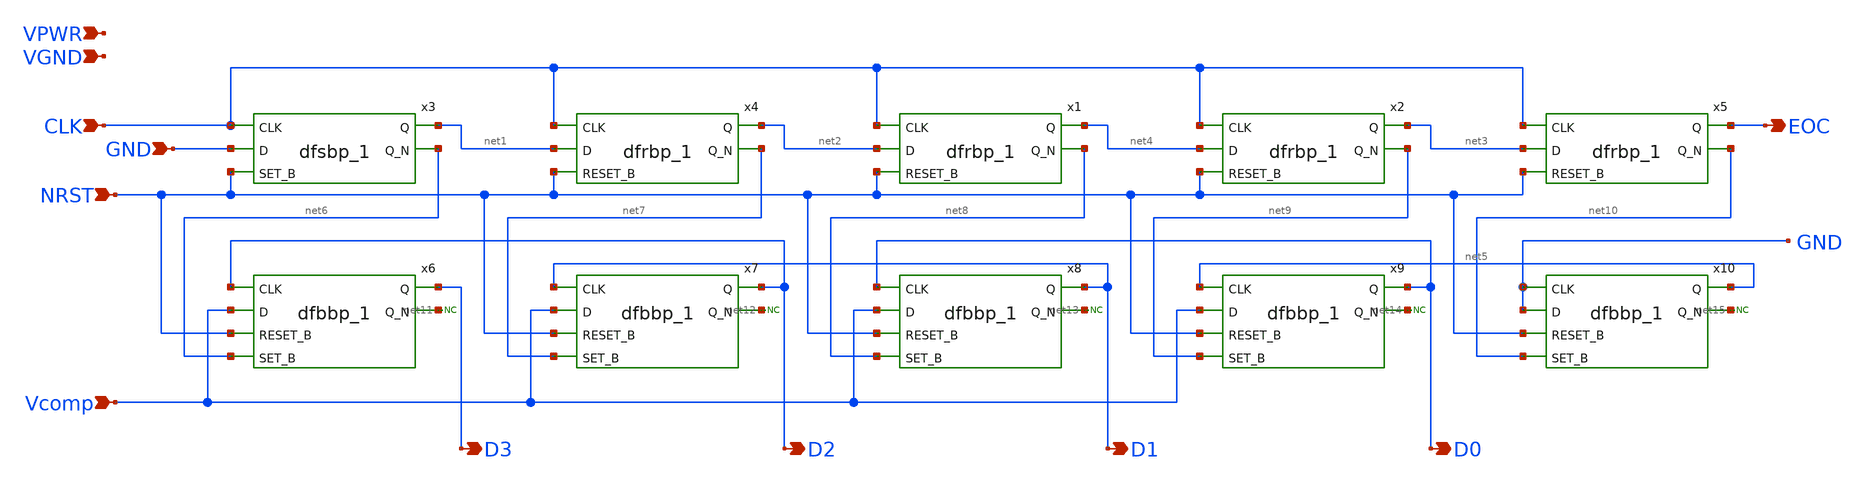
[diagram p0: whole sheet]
** sch_path: xschem/subckts/SAR.sch
**.subckt SAR NRST CLK EOC Vcomp D0 D1 D2 D3 GND VPWR VGND
*.ipin NRST
*.ipin CLK
*.opin EOC
*.ipin Vcomp
*.opin D0
*.opin D1
*.opin D2
*.opin D3
*.ipin GND
*.ipin VPWR
*.ipin VGND
x3 CLK GND NRST VGND VGND VPWR VPWR net1 net6 sky130_fd_sc_hd__dfsbp_1
x4 CLK net1 NRST VGND VGND VPWR VPWR net2 net7 sky130_fd_sc_hd__dfrbp_1
x1 CLK net2 NRST VGND VGND VPWR VPWR net4 net8 sky130_fd_sc_hd__dfrbp_1
x6 D2 Vcomp NRST net6 VGND VGND VPWR VPWR D3 net11 sky130_fd_sc_hd__dfbbp_1
x7 D1 Vcomp NRST net7 VGND VGND VPWR VPWR D2 net12 sky130_fd_sc_hd__dfbbp_1
x8 D0 Vcomp NRST net8 VGND VGND VPWR VPWR D1 net13 sky130_fd_sc_hd__dfbbp_1
x2 CLK net4 NRST VGND VGND VPWR VPWR net3 net9 sky130_fd_sc_hd__dfrbp_1
x5 CLK net3 NRST VGND VGND VPWR VPWR EOC net10 sky130_fd_sc_hd__dfrbp_1
x9 net5 Vcomp NRST net9 VGND VGND VPWR VPWR D0 net14 sky130_fd_sc_hd__dfbbp_1
x10 GND GND NRST net10 VGND VGND VPWR VPWR net5 net15 sky130_fd_sc_hd__dfbbp_1
* noconn #net11
* noconn #net12
* noconn #net13
* noconn #net14
* noconn #net15
**.ends
.end
